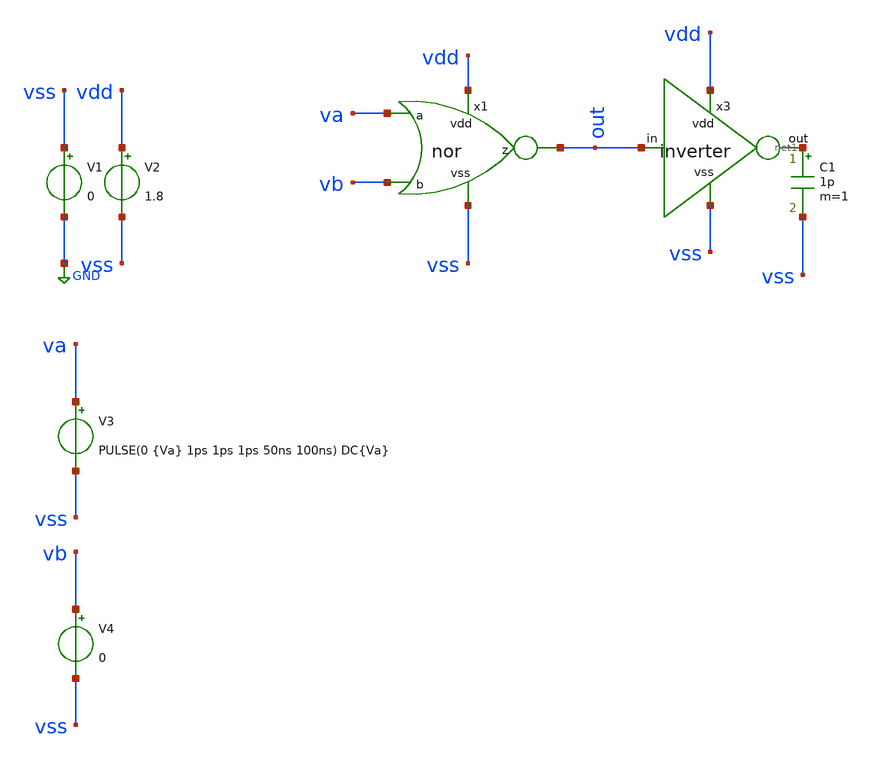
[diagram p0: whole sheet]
** sch_path: track_vlsi/ledesma/sch/tb_nor.sch
**.subckt tb_nor
V1 vss GND 0
V2 vdd vss 1.8
V3 va vss PULSE(0 {Va} 1ps 1ps 1ps 50ns 100ns) DC{Va}
V4 vb vss 0
x3 vdd net1 out vss inverter
C1 net1 vss 1p m=1
x1 vdd va vb out vss nor
**** begin user architecture code



* Parametros del circuito
.param Va=1.8
.param Vb=1.8
.options TEMP = 27.0

* Include
.lib /home/eamta/skywater/skywater-pdk/libraries/sky130_fd_pr_ngspice/latest/models/corners/sky130.lib TT

*simulation
.control
  tran 1p 200ns
  setplot tran1
  plot v(out) v(Va)+1.8 V(Vb)+3.6
  write tb_and_tran.raw

  reset
  dc V3 0 1.8 0.01
  setplot dc1
  plot v(out) v(Va)
  write tb_inverter_dc.ra

.endc
.end


**** end user architecture code
**.ends
.GLOBAL GND
.end
